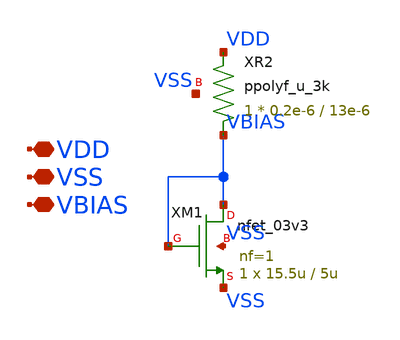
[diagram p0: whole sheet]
** sch_path: designs/libs/core_current-mirror/nbias-gen/nbias-gen.sch
**.subckt nbias-gen VDD VSS VBIAS
*.iopin VDD
*.iopin VSS
*.iopin VBIAS
XM1 VBIAS VBIAS VSS VSS nfet_03v3 L=5u W=15.5u nf=1 ad='int((nf+1)/2) * W/nf * 0.18u' as='int((nf+2)/2) * W/nf * 0.18u'
+ pd='2*int((nf+1)/2) * (W/nf + 0.18u)' ps='2*int((nf+2)/2) * (W/nf + 0.18u)' nrd='0.18u / W' nrs='0.18u / W'
+ sa=0 sb=0 sd=0 m=1
XR2 VBIAS VDD VSS ppolyf_u_3k r_width=0.2e-6 r_length=13e-6 m=1
**.ends
.end
